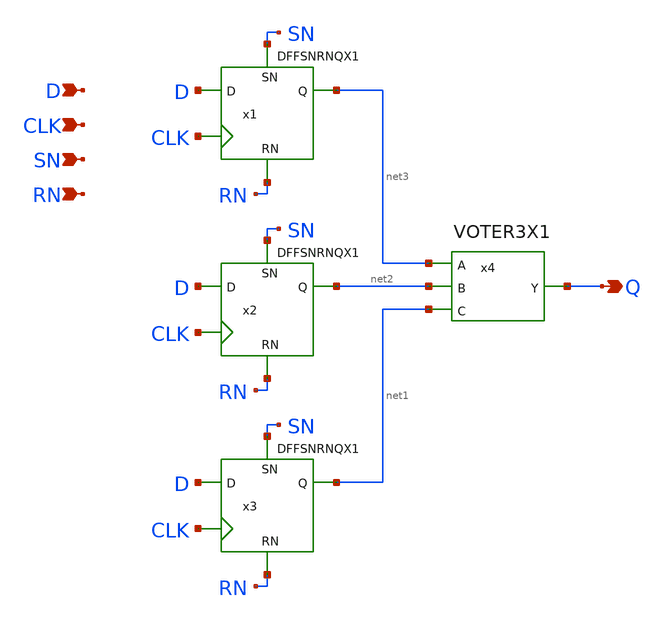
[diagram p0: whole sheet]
** sch_path: archives/lib/xschem/TMRDFFSNRNQX1.sch
**.subckt TMRDFFSNRNQX1 Q D CLK SN RN
*.opin Q
*.ipin D
*.ipin CLK
*.ipin SN
*.ipin RN
x1 net3 D CLK SN RN VDD VSS DFFSNRNQX1
x2 net2 D CLK SN RN VDD VSS DFFSNRNQX1
x3 net1 D CLK SN RN VDD VSS DFFSNRNQX1
x4 Q net3 net2 net1 VDD VSS VOTER3X1
**.ends
.end
